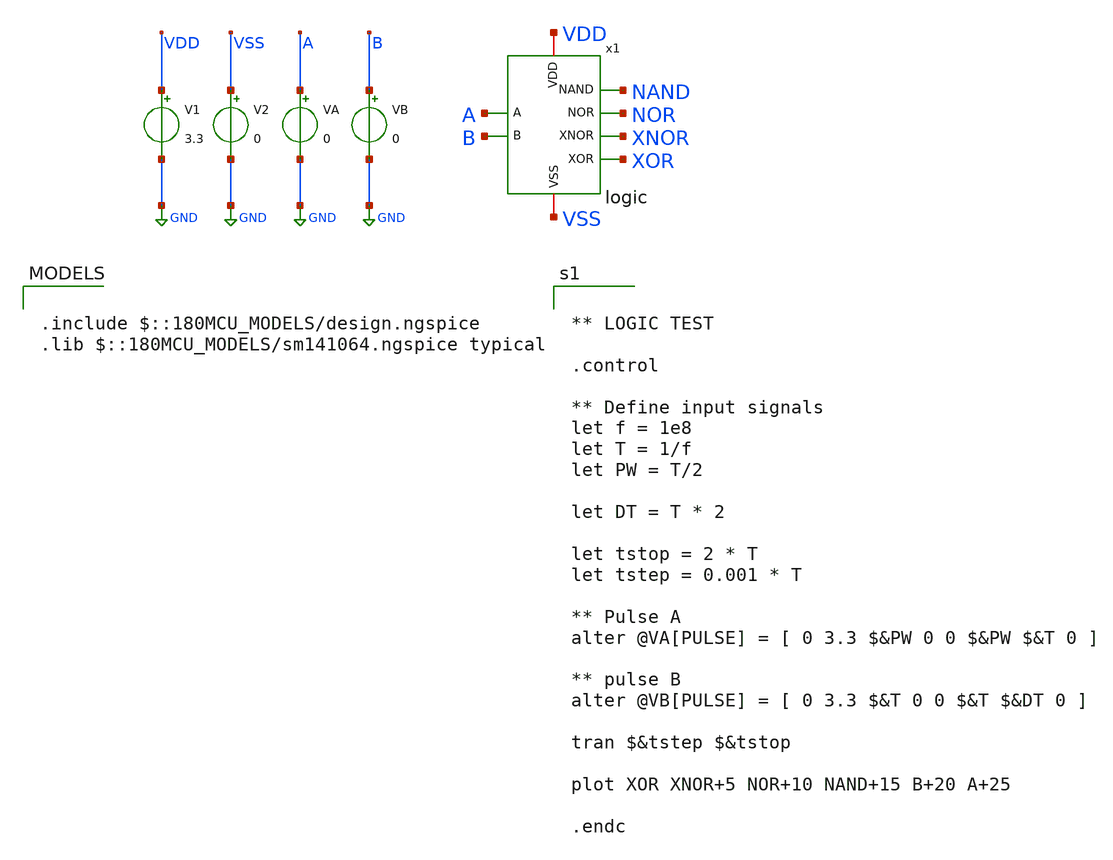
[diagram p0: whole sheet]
** sch_path: CAD4/logic_tb.sch
**.subckt logic_tb
x1 NOR VDD VSS XNOR A B NAND XOR logic
V1 VDD GND 3.3
V2 VSS GND 0
VA A GND 0
VB B GND 0
**** begin user architecture code


** LOGIC TEST

.control

** Define input signals
let f = 1e8
let T = 1/f
let PW = T/2

let DT = T * 2

let tstop = 2 * T
let tstep = 0.001 * T

** Pulse A
alter @VA[PULSE] = [ 0 3.3 $&PW 0 0 $&PW $&T 0 ]

** pulse B
alter @VB[PULSE] = [ 0 3.3 $&T 0 0 $&T $&DT 0 ]

tran $&tstep $&tstop

plot XOR XNOR+5 NOR+10 NAND+15 B+20 A+25

.endc



.include $::180MCU_MODELS/design.ngspice
.lib $::180MCU_MODELS/sm141064.ngspice typical

**** end user architecture code
**.ends
.GLOBAL GND
.end
